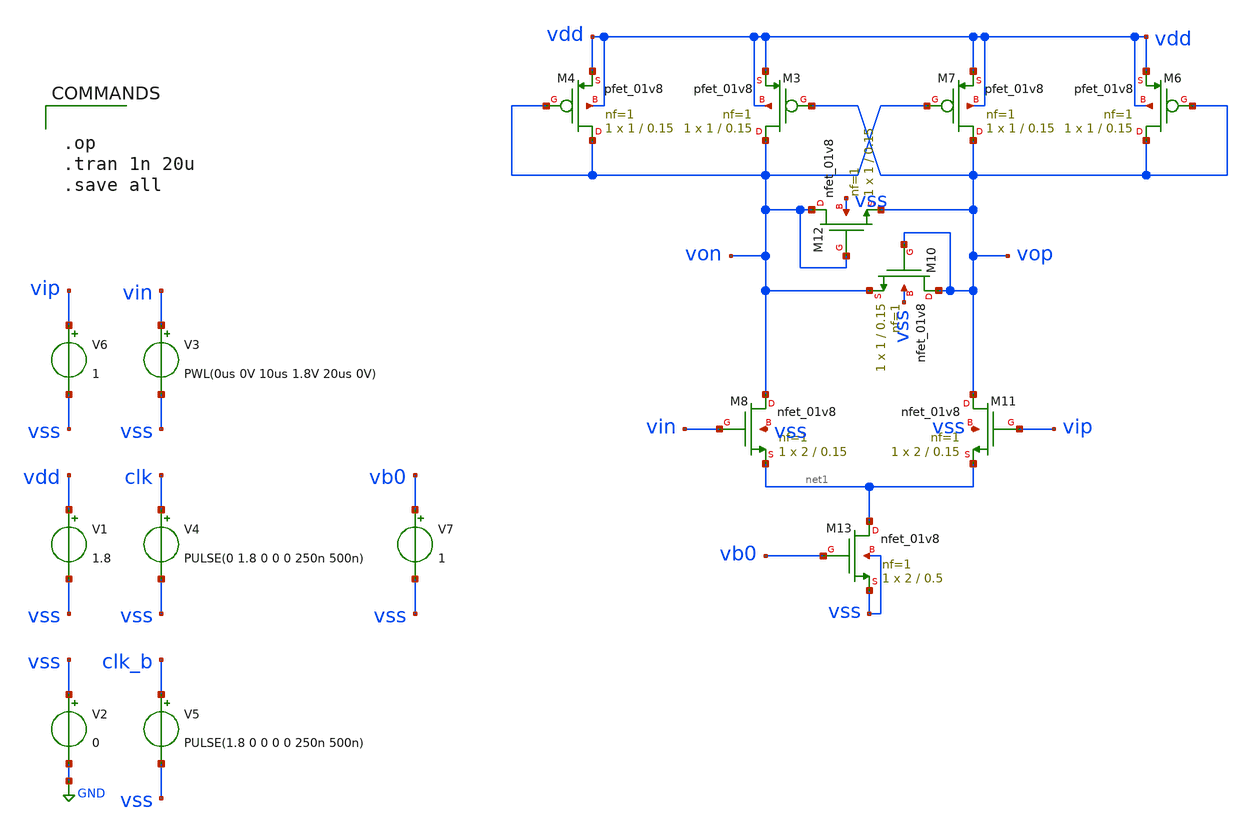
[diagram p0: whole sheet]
** sch_path: xschem/comparator/comparator_tb.sch
.lib $::SKYWATER_MODELS/sky130.lib.spice tt
.include $::SKYWATER_STDCELLS/sky130_fd_sc_hd.spice

**.subckt comparator_tb
V1 vdd vss 1.8
V3 vin vss PWL(0us 0V 10us 1.8V 20us 0V)
V4 clk vss PULSE(0 1.8 0 0 0 250n 500n)
V5 clk_b vss PULSE(1.8 0 0 0 0 250n 500n)
V6 vip vss 1
V2 vss GND 0
XM6 vop vop vdd vdd sky130_fd_pr__pfet_01v8 L=0.15 W=1 nf=1 ad='int((nf+1)/2) * W/nf * 0.29' as='int((nf+2)/2) * W/nf * 0.29'
+ pd='2*int((nf+1)/2) * (W/nf + 0.29)' ps='2*int((nf+2)/2) * (W/nf + 0.29)' nrd='0.29 / W' nrs='0.29 / W'
+ sa=0 sb=0 sd=0 mult=1 m=1
XM7 vop von vdd vdd sky130_fd_pr__pfet_01v8 L=0.15 W=1 nf=1 ad='int((nf+1)/2) * W/nf * 0.29' as='int((nf+2)/2) * W/nf * 0.29'
+ pd='2*int((nf+1)/2) * (W/nf + 0.29)' ps='2*int((nf+2)/2) * (W/nf + 0.29)' nrd='0.29 / W' nrs='0.29 / W'
+ sa=0 sb=0 sd=0 mult=1 m=1
XM3 von vop vdd vdd sky130_fd_pr__pfet_01v8 L=0.15 W=1 nf=1 ad='int((nf+1)/2) * W/nf * 0.29' as='int((nf+2)/2) * W/nf * 0.29'
+ pd='2*int((nf+1)/2) * (W/nf + 0.29)' ps='2*int((nf+2)/2) * (W/nf + 0.29)' nrd='0.29 / W' nrs='0.29 / W'
+ sa=0 sb=0 sd=0 mult=1 m=1
XM4 von von vdd vdd sky130_fd_pr__pfet_01v8 L=0.15 W=1 nf=1 ad='int((nf+1)/2) * W/nf * 0.29' as='int((nf+2)/2) * W/nf * 0.29'
+ pd='2*int((nf+1)/2) * (W/nf + 0.29)' ps='2*int((nf+2)/2) * (W/nf + 0.29)' nrd='0.29 / W' nrs='0.29 / W'
+ sa=0 sb=0 sd=0 mult=1 m=1
XM8 von vin net1 vss sky130_fd_pr__nfet_01v8 L=0.15 W=2 nf=1 ad='int((1 + 1)/2) * 2 / 1 * 0.29' as='int((1 + 2)/2) * 2 / 1 * 0.29'
+ pd='2*int((1 + 1)/2) * (2 / 1 + 0.29)' ps='2*int((1 + 2)/2) * (2 / 1 + 0.29)' nrd='0.29 / 2 ' nrs='0.29 / 2 '
+ sa=0 sb=0 sd=0 mult=1 m=1
XM10 vop vop von vss sky130_fd_pr__nfet_01v8 L=0.15 W=1 nf=1 ad='int((1 + 1)/2) * 1 / 1 * 0.29' as='int((1 + 2)/2) * 1 / 1 * 0.29'
+ pd='2*int((1 + 1)/2) * (1 / 1 + 0.29)' ps='2*int((1 + 2)/2) * (1 / 1 + 0.29)' nrd='0.29 / 1 ' nrs='0.29 / 1 '
+ sa=0 sb=0 sd=0 mult=1 m=1
XM11 vop vip net1 vss sky130_fd_pr__nfet_01v8 L=0.15 W=2 nf=1 ad='int((1 + 1)/2) * 2 / 1 * 0.29' as='int((1 + 2)/2) * 2 / 1 * 0.29'
+ pd='2*int((1 + 1)/2) * (2 / 1 + 0.29)' ps='2*int((1 + 2)/2) * (2 / 1 + 0.29)' nrd='0.29 / 2 ' nrs='0.29 / 2 '
+ sa=0 sb=0 sd=0 mult=1 m=1
XM12 von von vop vss sky130_fd_pr__nfet_01v8 L=0.15 W=1 nf=1 ad='int((1 + 1)/2) * 1 / 1 * 0.29' as='int((1 + 2)/2) * 1 / 1 * 0.29'
+ pd='2*int((1 + 1)/2) * (1 / 1 + 0.29)' ps='2*int((1 + 2)/2) * (1 / 1 + 0.29)' nrd='0.29 / 1 ' nrs='0.29 / 1 '
+ sa=0 sb=0 sd=0 mult=1 m=1
XM13 net1 vb0 vss vss sky130_fd_pr__nfet_01v8 L=0.5 W=2 nf=1 ad='int((1 + 1)/2) * 2 / 1 * 0.29' as='int((1 + 2)/2) * 2 / 1 * 0.29'
+ pd='2*int((1 + 1)/2) * (2 / 1 + 0.29)' ps='2*int((1 + 2)/2) * (2 / 1 + 0.29)' nrd='0.29 / 2 ' nrs='0.29 / 2 '
+ sa=0 sb=0 sd=0 mult=1 m=1
V7 vb0 vss 1
**** begin user architecture code


.op
.tran 1n 20u
.save all


**** end user architecture code
**.ends
.GLOBAL GND
.end
